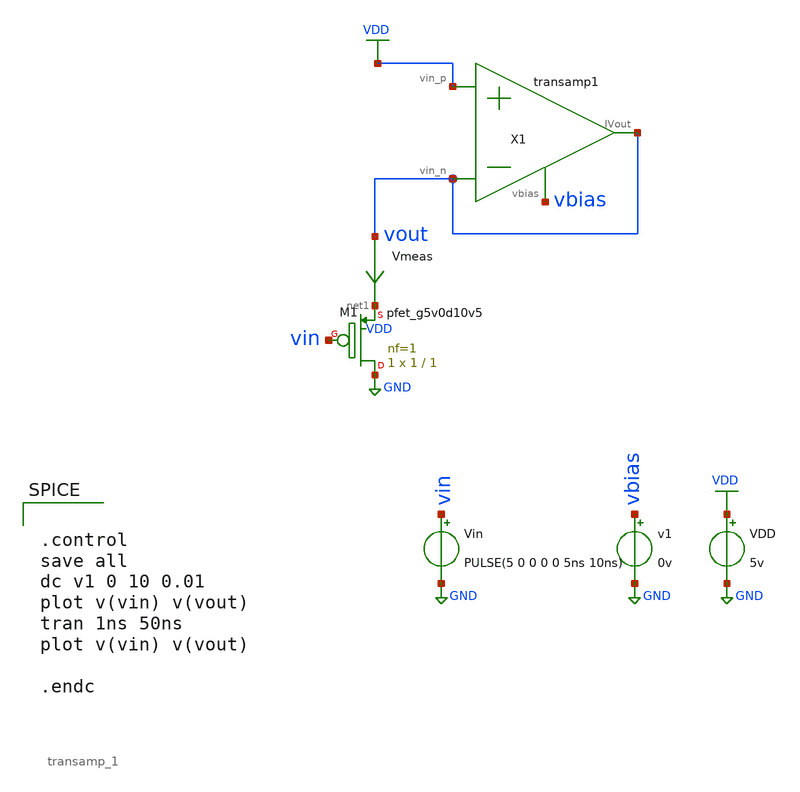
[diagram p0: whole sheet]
** sch_path: schematics/CS_amp_tb.sch
**.subckt CS_amp_tb
VDD VDD GND 5v
v1 vbias GND 0v
Vin vin GND PULSE(5 0 0 0 0 5ns 10ns)
Vmeas vout net1 0
.save i(vmeas)
XM1 GND vin net1 VDD sky130_fd_pr__pfet_g5v0d10v5 L=1 W=1 nf=1 ad='int((nf+1)/2) * W/nf * 0.29' as='int((nf+2)/2) * W/nf * 0.29'
+ pd='2*int((nf+1)/2) * (W/nf + 0.29)' ps='2*int((nf+2)/2) * (W/nf + 0.29)' nrd='0.29 / W' nrs='0.29 / W'
+ sa=0 sb=0 sd=0 mult=1 m=1
X1 VDD vout vout vbias transamp_1
**** begin user architecture code


.control
save all
dc v1 0 10 0.01
plot v(vin) v(vout)
tran 1ns 50ns
plot v(vin) v(vout)

.endc


 .lib $::SKYWATER_MODELS/models/sky130.lib.spice tt

.param mc_mm_switch=0
.param mc_pr_switch=1

**** end user architecture code
**.ends

* expanding   symbol:  /media/sf_share/final_project/transamp_1.sym # of pins=4
** sym_path: schematics/transamp_1.sym
** sch_path: schematics/transamp_1.sch
.subckt transamp_1 vin_p vin_n IVout vbias
*.opin IVout
*.ipin vin_p
*.ipin vin_n
*.ipin vbias
XM1 net1 vbias GND GND sky130_fd_pr__nfet_g5v0d10v5 L=1 W=1 nf=1 ad='int((nf+1)/2) * W/nf * 0.29' as='int((nf+2)/2) * W/nf * 0.29'
+ pd='2*int((nf+1)/2) * (W/nf + 0.29)' ps='2*int((nf+2)/2) * (W/nf + 0.29)' nrd='0.29 / W' nrs='0.29 / W'
+ sa=0 sb=0 sd=0 mult=1 m=1
XM3 net2 vin_p net1 GND sky130_fd_pr__nfet_g5v0d10v5 L=1 W=1 nf=1 ad='int((nf+1)/2) * W/nf * 0.29' as='int((nf+2)/2) * W/nf * 0.29'
+ pd='2*int((nf+1)/2) * (W/nf + 0.29)' ps='2*int((nf+2)/2) * (W/nf + 0.29)' nrd='0.29 / W' nrs='0.29 / W'
+ sa=0 sb=0 sd=0 mult=1 m=1
XM4 IVout net2 VDD VDD sky130_fd_pr__pfet_g5v0d10v5 L=1 W=1 nf=1 ad='int((nf+1)/2) * W/nf * 0.29' as='int((nf+2)/2) * W/nf * 0.29'
+ pd='2*int((nf+1)/2) * (W/nf + 0.29)' ps='2*int((nf+2)/2) * (W/nf + 0.29)' nrd='0.29 / W' nrs='0.29 / W'
+ sa=0 sb=0 sd=0 mult=1 m=1
XM2 IVout vin_n net1 GND sky130_fd_pr__nfet_g5v0d10v5 L=1 W=1 nf=1 ad='int((nf+1)/2) * W/nf * 0.29' as='int((nf+2)/2) * W/nf * 0.29'
+ pd='2*int((nf+1)/2) * (W/nf + 0.29)' ps='2*int((nf+2)/2) * (W/nf + 0.29)' nrd='0.29 / W' nrs='0.29 / W'
+ sa=0 sb=0 sd=0 mult=1 m=1
XM5 net2 net2 VDD VDD sky130_fd_pr__pfet_g5v0d10v5 L=1 W=1 nf=1 ad='int((nf+1)/2) * W/nf * 0.29' as='int((nf+2)/2) * W/nf * 0.29'
+ pd='2*int((nf+1)/2) * (W/nf + 0.29)' ps='2*int((nf+2)/2) * (W/nf + 0.29)' nrd='0.29 / W' nrs='0.29 / W'
+ sa=0 sb=0 sd=0 mult=1 m=1
.ends

.GLOBAL VDD
.GLOBAL GND
.end
